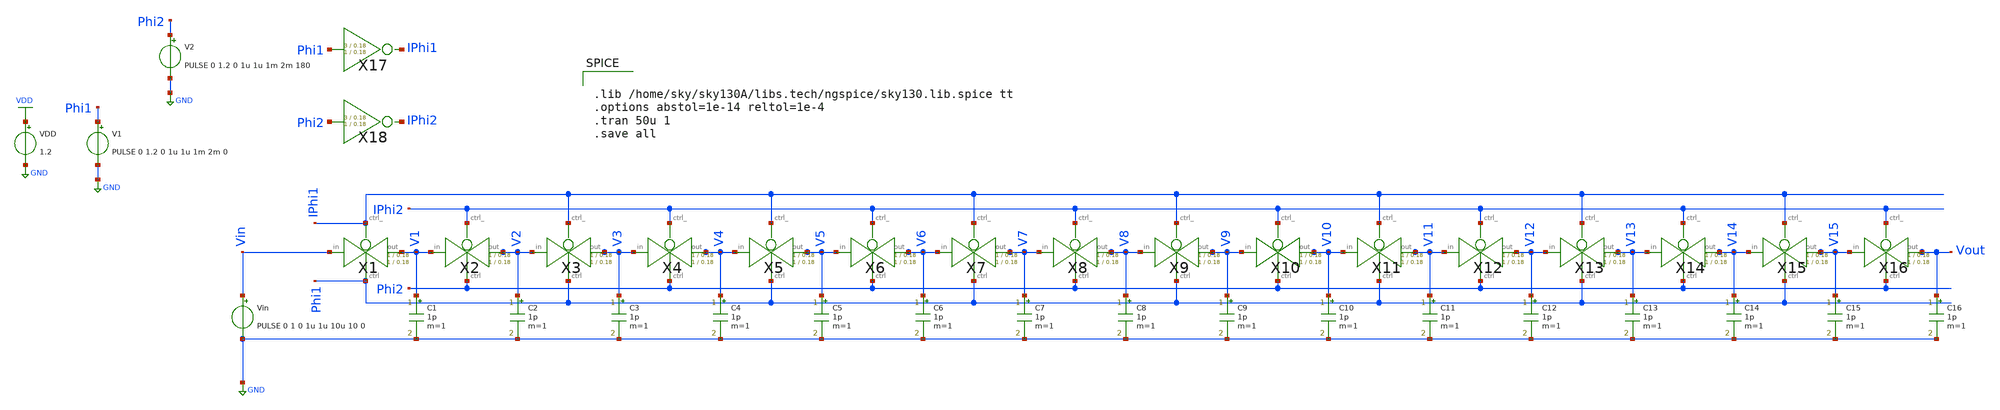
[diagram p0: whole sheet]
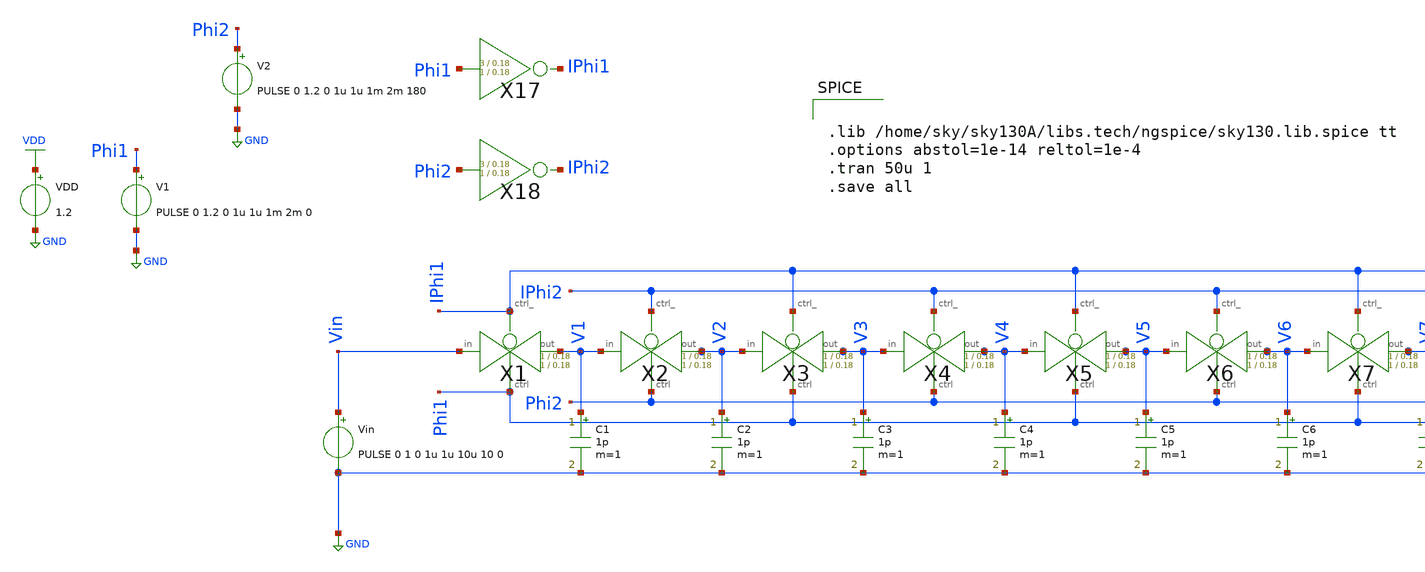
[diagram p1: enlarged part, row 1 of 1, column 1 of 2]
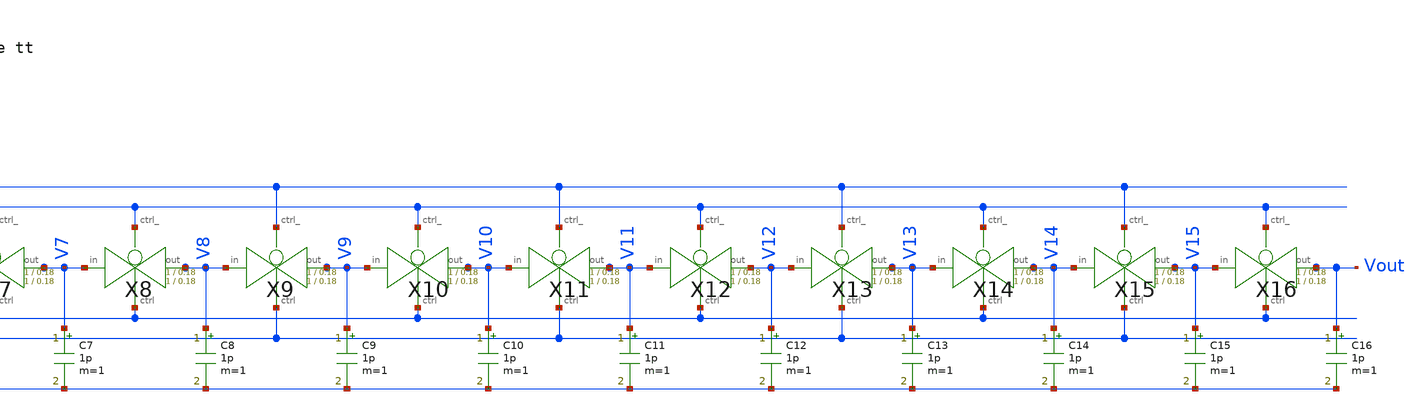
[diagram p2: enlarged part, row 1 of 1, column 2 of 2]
** sch_path: xschem/Switched_Caps/Single_Line.sch.sch
**.subckt Single_Line.sch
X1 Vin V1 IPhi1 Phi1 transmission_gate Wpmos=1 Lpmos=0.18 Wnmos=1 Lnmos=0.18
X2 V1 V2 IPhi2 Phi2 transmission_gate Wpmos=1 Lpmos=0.18 Wnmos=1 Lnmos=0.18
X3 V2 V3 IPhi1 Phi1 transmission_gate Wpmos=1 Lpmos=0.18 Wnmos=1 Lnmos=0.18
X4 V3 V4 IPhi2 Phi2 transmission_gate Wpmos=1 Lpmos=0.18 Wnmos=1 Lnmos=0.18
X5 V4 V5 IPhi1 Phi1 transmission_gate Wpmos=1 Lpmos=0.18 Wnmos=1 Lnmos=0.18
X6 V5 V6 IPhi2 Phi2 transmission_gate Wpmos=1 Lpmos=0.18 Wnmos=1 Lnmos=0.18
X7 V6 V7 IPhi1 Phi1 transmission_gate Wpmos=1 Lpmos=0.18 Wnmos=1 Lnmos=0.18
X8 V7 V8 IPhi2 Phi2 transmission_gate Wpmos=1 Lpmos=0.18 Wnmos=1 Lnmos=0.18
X9 V8 V9 IPhi1 Phi1 transmission_gate Wpmos=1 Lpmos=0.18 Wnmos=1 Lnmos=0.18
X10 V9 V10 IPhi2 Phi2 transmission_gate Wpmos=1 Lpmos=0.18 Wnmos=1 Lnmos=0.18
X11 V10 V11 IPhi1 Phi1 transmission_gate Wpmos=1 Lpmos=0.18 Wnmos=1 Lnmos=0.18
X12 V11 V12 IPhi2 Phi2 transmission_gate Wpmos=1 Lpmos=0.18 Wnmos=1 Lnmos=0.18
X13 V12 V13 IPhi1 Phi1 transmission_gate Wpmos=1 Lpmos=0.18 Wnmos=1 Lnmos=0.18
X14 V13 V14 IPhi2 Phi2 transmission_gate Wpmos=1 Lpmos=0.18 Wnmos=1 Lnmos=0.18
X15 V14 V15 IPhi1 Phi1 transmission_gate Wpmos=1 Lpmos=0.18 Wnmos=1 Lnmos=0.18
X16 V15 Vout IPhi2 Phi2 transmission_gate Wpmos=1 Lpmos=0.18 Wnmos=1 Lnmos=0.18
V1 Phi1 GND PULSE 0 1.2 0 1u 1u 1m 2m 0
V2 Phi2 GND PULSE 0 1.2 0 1u 1u 1m 2m 180
Vin Vin GND PULSE 0 1 0 1u 1u 10u 10 0
C1 V1 GND 1p m=1
C2 V2 GND 1p m=1
C3 V3 GND 1p m=1
C4 V4 GND 1p m=1
C5 V5 GND 1p m=1
C6 V6 GND 1p m=1
C7 V7 GND 1p m=1
C8 V8 GND 1p m=1
C9 V9 GND 1p m=1
C10 V10 GND 1p m=1
C11 V11 GND 1p m=1
C12 V12 GND 1p m=1
C13 V13 GND 1p m=1
C14 V14 GND 1p m=1
C15 V15 GND 1p m=1
C16 Vout GND 1p m=1
X17 Phi1 IPhi1 inv Wpmos=3 Lpmos=0.18 Wnmos=1 Lnmos=0.18
X18 Phi2 IPhi2 inv Wpmos=3 Lpmos=0.18 Wnmos=1 Lnmos=0.18
VDD VDD GND 1.2
**** begin user architecture code


.lib /home/sky/sky130A/libs.tech/ngspice/sky130.lib.spice tt
.options abstol=1e-14 reltol=1e-4
.tran 50u 1
.save all


**** end user architecture code
**.ends

* expanding   symbol:  transmission_gate/transmission_gate.sym # of pins=4
** sym_path: xschem/transmission_gate/transmission_gate.sym
** sch_path: xschem/transmission_gate/transmission_gate.sch
.subckt transmission_gate in out ctrl_ ctrl  Wpmos=1 Lpmos=0.18 Wnmos=1 Lnmos=0.18
*.iopin in
*.iopin out
*.ipin ctrl_
*.ipin ctrl
XM1 in ctrl out GND sky130_fd_pr__nfet_01v8 L=Lnmos W=Wnmos nf=1 ad='int((nf+1)/2) * W/nf * 0.29' as='int((nf+2)/2) * W/nf * 0.29'
+ pd='2*int((nf+1)/2) * (W/nf + 0.29)' ps='2*int((nf+2)/2) * (W/nf + 0.29)' nrd='0.29 / W' nrs='0.29 / W'
+ sa=0 sb=0 sd=0 mult=1 m=1
XM2 out ctrl_ in VDD sky130_fd_pr__pfet_01v8 L=Lpmos W=Wpmos nf=1 ad='int((nf+1)/2) * W/nf * 0.29' as='int((nf+2)/2) * W/nf * 0.29'
+ pd='2*int((nf+1)/2) * (W/nf + 0.29)' ps='2*int((nf+2)/2) * (W/nf + 0.29)' nrd='0.29 / W' nrs='0.29 / W'
+ sa=0 sb=0 sd=0 mult=1 m=1
.ends


* expanding   symbol:  inv/inv.sym # of pins=2
** sym_path: xschem/inv/inv.sym
** sch_path: xschem/inv/inv.sch
.subckt inv in out  Wpmos=3 Lpmos=0.18 Wnmos=1 Lnmos=0.18
*.ipin in
*.iopin out
XM1 out in GND GND sky130_fd_pr__nfet_01v8 L=Lnmos W=Wnmos nf=1 ad='int((nf+1)/2) * W/nf * 0.29' as='int((nf+2)/2) * W/nf * 0.29'
+ pd='2*int((nf+1)/2) * (W/nf + 0.29)' ps='2*int((nf+2)/2) * (W/nf + 0.29)' nrd='0.29 / W' nrs='0.29 / W'
+ sa=0 sb=0 sd=0 mult=1 m=1
XM2 out in VDD VDD sky130_fd_pr__pfet_01v8 L=Lpmos W=Wpmos nf=1 ad='int((nf+1)/2) * W/nf * 0.29' as='int((nf+2)/2) * W/nf * 0.29'
+ pd='2*int((nf+1)/2) * (W/nf + 0.29)' ps='2*int((nf+2)/2) * (W/nf + 0.29)' nrd='0.29 / W' nrs='0.29 / W'
+ sa=0 sb=0 sd=0 mult=1 m=1
.ends

.GLOBAL GND
.GLOBAL VDD
.end
